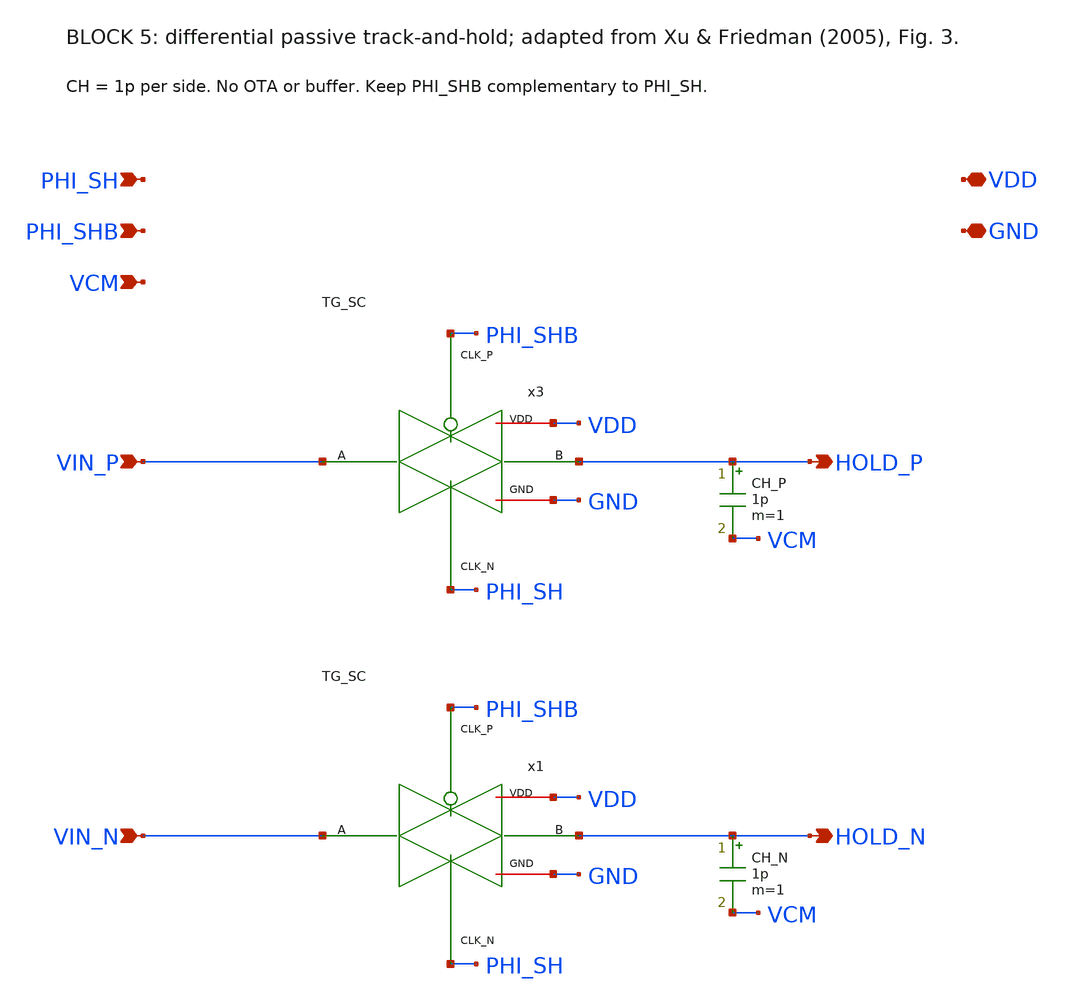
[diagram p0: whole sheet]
** sch_path: blocks/05_Switch_Network/xschem/Block5_SH.sch
**.subckt Block5_SH VIN_P VIN_N PHI_SH PHI_SHB VDD GND VCM HOLD_P HOLD_N
*.ipin VIN_P
*.ipin VIN_N
*.ipin PHI_SH
*.ipin PHI_SHB
*.iopin VDD
*.iopin GND
*.ipin VCM
*.opin HOLD_P
*.opin HOLD_N
CH_P HOLD_P VCM 1p m=1
CH_N HOLD_N VCM 1p m=1
x3 VIN_P HOLD_P PHI_SHB PHI_SH VDD GND TG_SC
x1 VIN_N HOLD_N PHI_SHB PHI_SH VDD GND TG_SC
**.ends

* expanding   symbol:  blocks/05_Switch_Network/xschem/TG_SC.sym # of pins=6
** sym_path: blocks/05_Switch_Network/xschem/TG_SC.sym
** sch_path: blocks/05_Switch_Network/xschem/TG_SC.sch
.subckt TG_SC A B CLK_P CLK_N VDD GND
*.iopin A
*.iopin B
*.ipin CLK_P
*.ipin CLK_N
*.iopin VDD
*.iopin GND
XMP A CLK_P B VDD sky130_fd_pr__pfet_01v8 L=0.15 W=4 nf=1 ad='int((1 + 1)/2) * 4 / 1 * 0.29' as='int((1 + 2)/2) * 4 / 1 * 0.29'
+ pd='2*int((1 + 1)/2) * (4 / 1 + 0.29)' ps='2*int((1 + 2)/2) * (4 / 1 + 0.29)' nrd='0.29 / 4 ' nrs='0.29 / 4 '
+ sa=0 sb=0 sd=0 mult=1 m=1
XMN A CLK_N B GND sky130_fd_pr__nfet_01v8 L=0.15 W=2 nf=1 ad='int((1 + 1)/2) * 2 / 1 * 0.29' as='int((1 + 2)/2) * 2 / 1 * 0.29'
+ pd='2*int((1 + 1)/2) * (2 / 1 + 0.29)' ps='2*int((1 + 2)/2) * (2 / 1 + 0.29)' nrd='0.29 / 2 ' nrs='0.29 / 2 '
+ sa=0 sb=0 sd=0 mult=1 m=1
.ends

.end
